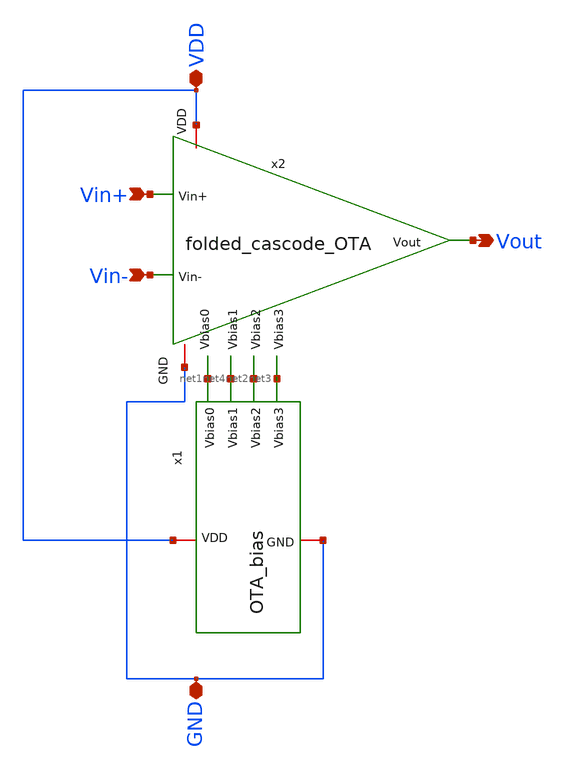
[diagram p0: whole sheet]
** sch_path: analog/B04_OTA_biased.sch
**.subckt B04_OTA_biased VDD GND Vin+ Vin- Vout
*.iopin VDD
*.iopin GND
*.ipin Vin+
*.ipin Vin-
*.opin Vout
x1 VDD net1 net2 net3 net4 GND OTA_bias cur_factor=1
x2 VDD net1 Vin+ Vin- net3 net4 Vout net2 GND folded_cascode_OTA
**.ends
.end
